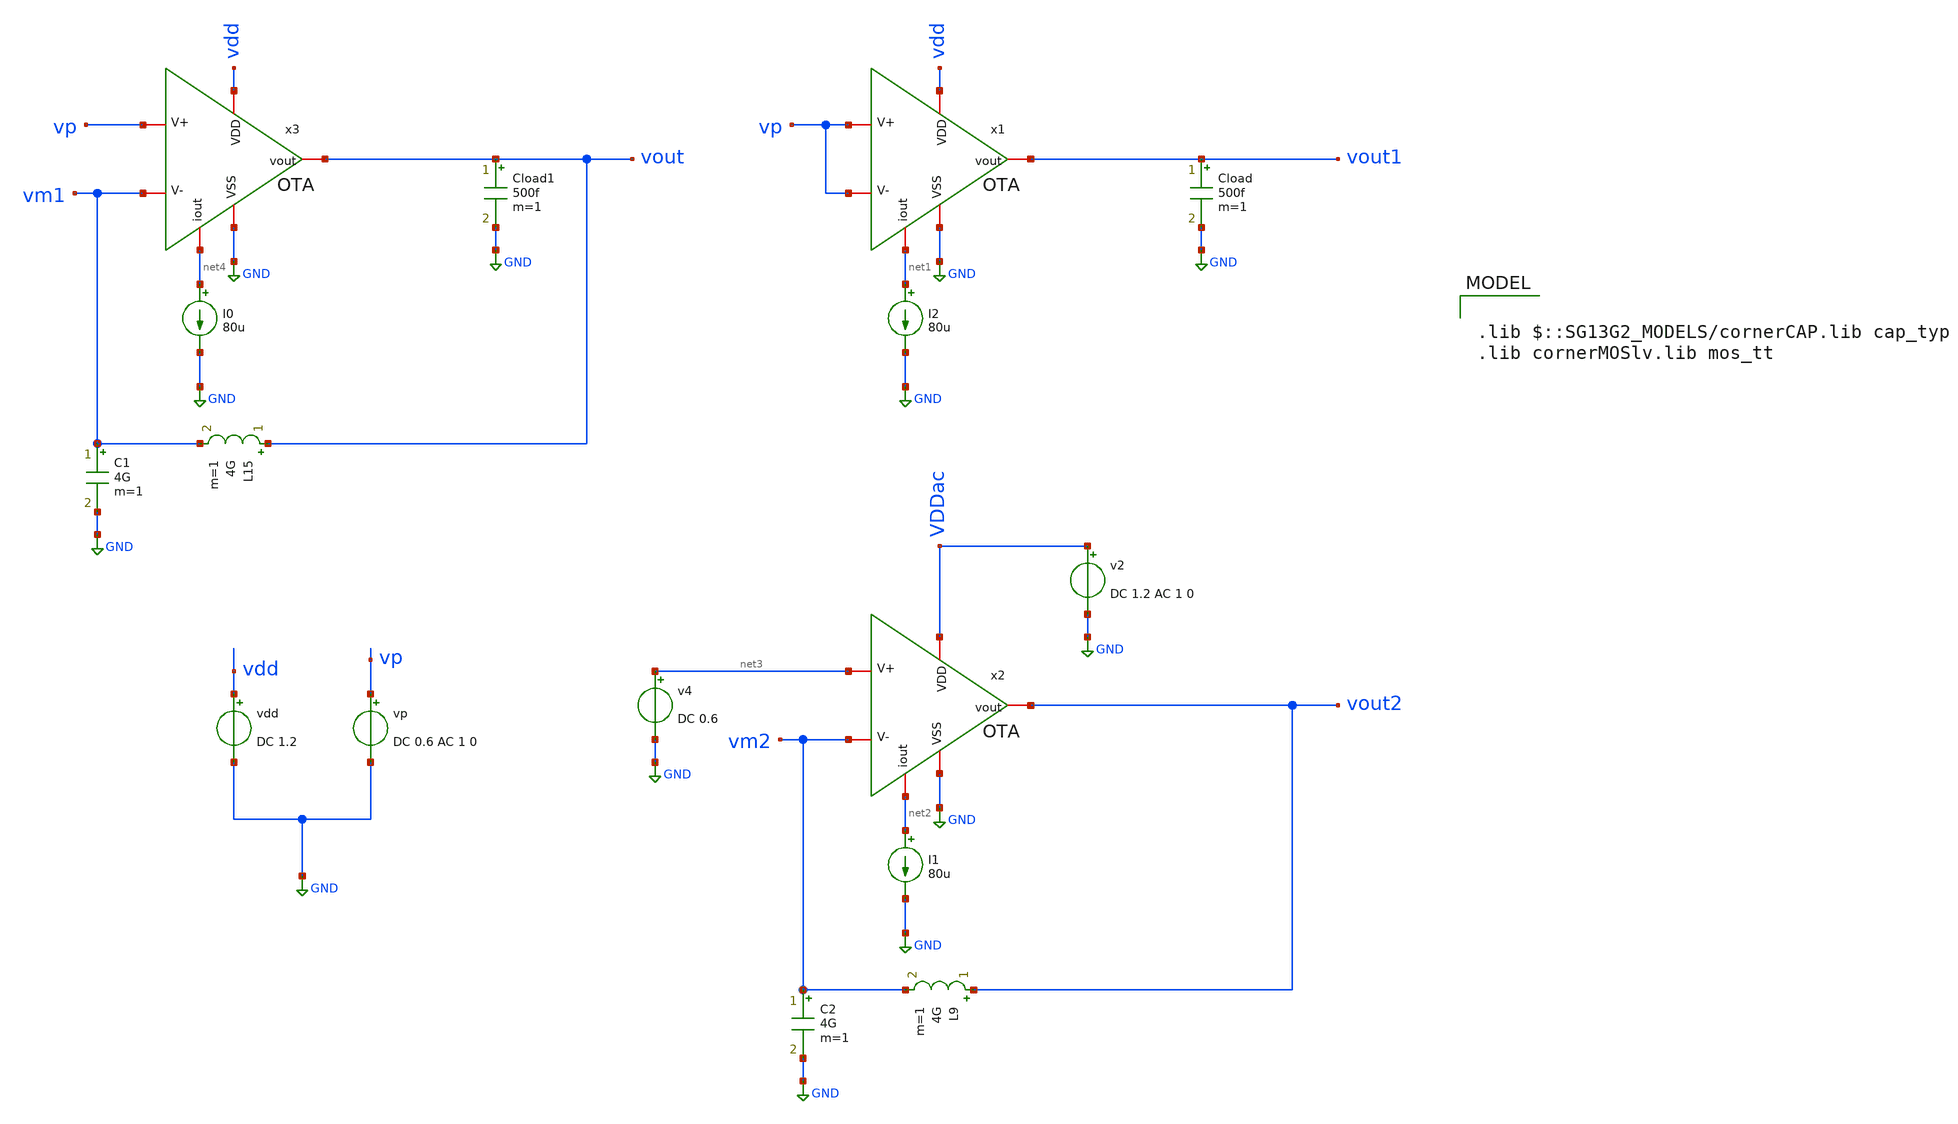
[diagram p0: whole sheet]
** sch_path: BTDay7-Ex/TestCMRR_PSRR-OTA.sch
**.subckt TestCMRR_PSRR-OTA
I2 net1 GND 80u
Cload vout1 GND 500f m=1
vdd vdd GND DC 1.2
vp vp GND DC 0.6 AC 1 0
x1 vp vp GND vdd net1 vout1 OTA
I1 net2 GND 80u
C2 vm2 GND 4G m=1
L9 vout2 vm2 4G m=1
x2 vm2 net3 GND VDDac net2 vout2 OTA
v4 net3 GND DC 0.6
v2 VDDac GND DC 1.2 AC 1 0
I0 net4 GND 80u
Cload1 vout GND 500f m=1
C1 vm1 GND 4G m=1
L15 vout vm1 4G m=1
x3 vm1 vp GND vdd net4 vout OTA
**** begin user architecture code

.lib $::SG13G2_MODELS/cornerCAP.lib cap_typ
.lib cornerMOSlv.lib mos_tt




.control
op
save all

* Chay phan tich AC tu 1Hz den 10MHz
ac dec 100 1 10e6
save all

* Tinh toan cac dai luong theo Slide 23
let Av = db(v(vout))
let PSRR = db(v(vout2)/v(VDDac))
let CMRR = db((v(vout)/v(vp))/(v(vout1)/v(vp)))
let phase = 180*cph(vout)/pi

* Ghi du lieu ra file raw
write output_file.raw

* Ve do thi kiem tra truc tiep tren Ngspice
plot CMRR xlog title 'Common-Mode Rejection Ratio - CMRR (dB)'
plot PSRR xlog title 'Power Supply Rejection Ratio - PSRR (dB)'
.endc


**** end user architecture code
**.ends

* expanding   symbol:  /foss/designs/BTDay7-Ex/OTA.sym # of pins=6
** sym_path: BTDay7-Ex/OTA.sym
** sch_path: BTDay7-Ex/OTA.sch
.subckt OTA V- V+ VSS VDD iout vout
*.iopin VDD
*.iopin iout
*.iopin V-
*.iopin VSS
*.iopin V+
*.iopin vout
XM6 iout iout VDD VDD sg13_lv_pmos w=75u l=2.08u ng=8 m=1 mm_ok=1
XM7 net1 iout VDD VDD sg13_lv_pmos w=5.3u l=1.95u ng=1 m=1 mm_ok=1
XM8 net3 V- net1 VDD sg13_lv_pmos w=7.41u l=3.64u ng=1 m=1 mm_ok=1
XM9 net2 V+ net1 VDD sg13_lv_pmos w=7.41u l=3.64u ng=1 m=1 mm_ok=1
XM10 net3 net3 VSS VSS sg13_lv_nmos w=720n l=9.75u ng=1 m=1 mm_ok=1
XM11 net2 net3 VSS VSS sg13_lv_nmos w=720n l=9.75u ng=1 m=1 mm_ok=1
XM1 vout net2 VSS VSS sg13_lv_nmos w=28.8u l=9.75u ng=4 m=1 mm_ok=1
XM2 vout iout VDD VDD sg13_lv_pmos w=75u l=2.08u ng=8 m=1 mm_ok=1
XC1 net2 vout cap_cmim w=22.295e-6 l=22.295e-6 m=1 mm_ok=1
.ends

.GLOBAL GND
.end
